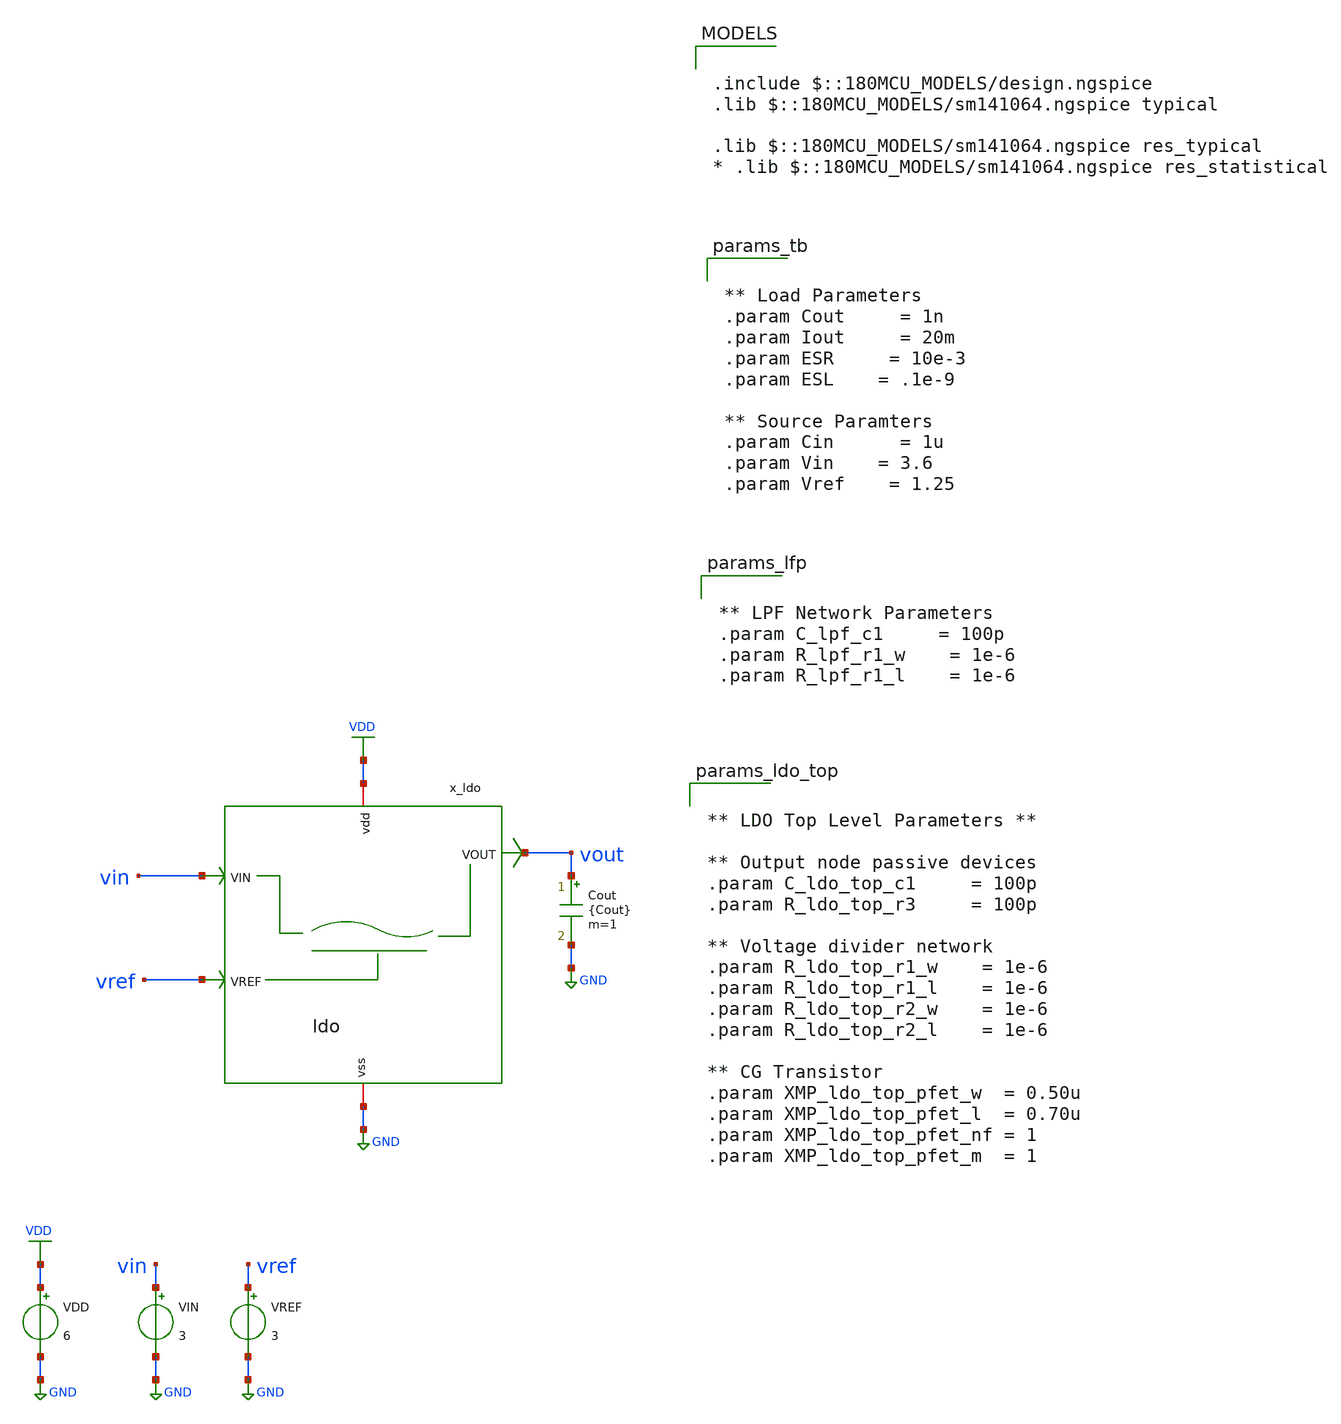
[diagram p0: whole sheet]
** sch_path: analog-db/circuits/ldo_005_buffered_ref/reference/ti-ldo/testbench/dc_trans_tb.sch
**.subckt dc_trans_tb
VDD VDD GND 6
VIN vin GND 3
VREF vref GND 3
Cout vout GND {Cout} m=1
x_ldo vout vin vref GND VDD ldo
**** begin user architecture code

.include $::180MCU_MODELS/design.ngspice
.lib $::180MCU_MODELS/sm141064.ngspice typical

.lib $::180MCU_MODELS/sm141064.ngspice res_typical
* .lib $::180MCU_MODELS/sm141064.ngspice res_statistical


** Load Parameters
.param Cout 	= 1n
.param Iout 	= 20m
.param ESR 	= 10e-3
.param ESL	= .1e-9

** Source Paramters
.param Cin  	= 1u
.param Vin	= 3.6
.param Vref	= 1.25



** LPF Network Parameters
.param C_lpf_c1 	= 100p
.param R_lpf_r1_w	= 1e-6
.param R_lpf_r1_l	= 1e-6



** LDO Top Level Parameters **

** Output node passive devices
.param C_ldo_top_c1 	= 100p
.param R_ldo_top_r3 	= 100p

** Voltage divider network
.param R_ldo_top_r1_w	= 1e-6
.param R_ldo_top_r1_l	= 1e-6
.param R_ldo_top_r2_w	= 1e-6
.param R_ldo_top_r2_l	= 1e-6

** CG Transistor
.param XMP_ldo_top_pfet_w  = 0.50u
.param XMP_ldo_top_pfet_l  = 0.70u
.param XMP_ldo_top_pfet_nf = 1
.param XMP_ldo_top_pfet_m  = 1




** Ref Amp Parameters **

.param I_ref_ref_amp = 1m


** Passive Devices
.param C_ref_amp_c1 	= 100p

.param R_ref_amp_r1_w	= 1e-6
.param R_ref_amp_r1_l	= 1e-6

** NMOS
** ref_amp.M1 Transistor
.param M1_ref_amp_nfet_w  = 0.50u
.param M1_ref_amp_nfet_l  = 0.30u
.param M1_ref_amp_nfet_nf = 1
.param M1_ref_amp_nfet_m  = 1

** ref_amp.M2 Transistor
.param M2_ref_amp_nfet_w  = 0.50u
.param M2_ref_amp_nfet_l  = 0.30u
.param M2_ref_amp_nfet_nf = 1
.param M2_ref_amp_nfet_m  = 1

** ref_amp.M_mirror_out Transistor
.param M_mirror_out_ref_amp_nfet_w  = 0.50u
.param M_mirror_out_ref_amp_nfet_l  = 0.30u
.param M_mirror_out_ref_amp_nfet_nf = 1
.param M_mirror_out_ref_amp_nfet_m  = 1

** ref_amp.M_mirror_a Transistor
.param M_mirror_a_ref_amp_nfet_w  = 0.50u
.param M_mirror_a_ref_amp_nfet_l  = 0.30u
.param M_mirror_a_ref_amp_nfet_nf = 1
.param M_mirror_a_ref_amp_nfet_m  = 1


** ref_amp.M_mirror_ref Transistor
.param M_mirror_ref_ref_amp_nfet_w  = 0.50u
.param M_mirror_ref_ref_amp_nfet_l  = 0.30u
.param M_mirror_ref_ref_amp_nfet_nf = 1
.param M_mirror_ref_ref_amp_nfet_m  = 1


** PMOS
** ref_amp.M3 Transistor
.param M3_ref_amp_pfet_w  = 0.50u
.param M3_ref_amp_pfet_l  = 0.30u
.param M3_ref_amp_pfet_nf = 1
.param M3_ref_amp_pfet_m  = 1


** ref_amp.M4 Transistor
.param M4_ref_amp_pfet_w  = 0.50u
.param M4_ref_amp_pfet_l  = 0.30u
.param M4_ref_amp_pfet_nf = 1
.param M4_ref_amp_pfet_m  = 1


** ref_amp.M5 Transistor
.param M5_ref_amp_pfet_w  = 0.50u
.param M5_ref_amp_pfet_l  = 0.30u
.param M5_ref_amp_pfet_nf = 1
.param M5_ref_amp_pfet_m  = 1



** Error Amp Parameters **

.param I_error_amp_ref = 1m


** Passive Devices
.param C_error_amp_cc 	= 100p

.param R_error_amp_rz_w	= 1e-6
.param R_error_amp_rz_l	= 1e-6

** NMOS
** error_amp.M1 Transistor
.param M1_error_amp_nfet_w  = 0.50u
.param M1_error_amp_nfet_l  = 0.30u
.param M1_error_amp_nfet_nf = 1
.param M1_error_amp_nfet_m  = 1

** error_amp.M2 Transistor
.param M2_error_amp_nfet_w  = 0.50u
.param M2_error_amp_nfet_l  = 0.30u
.param M2_error_amp_nfet_nf = 1
.param M2_error_amp_nfet_m  = 1

** error_amp.M_mirror_ea_out Transistor
.param M_mirror_ea_out_error_amp_nfet_w  = 0.50u
.param M_mirror_ea_out_error_amp_nfet_l  = 0.30u
.param M_mirror_ea_out_error_amp_nfet_nf = 1
.param M_mirror_ea_out_error_amp_nfet_m  = 1

** error_amp.M_mirror_e Transistor
.param M_mirror_e_error_amp_nfet_w  = 0.50u
.param M_mirror_e_error_amp_nfet_l  = 0.30u
.param M_mirror_e_error_amp_nfet_nf = 1
.param M_mirror_e_error_amp_nfet_m  = 1

** error_amp.M_mirror_c Transistor
.param M_mirror_c_error_amp_nfet_w  = 0.50u
.param M_mirror_c_error_amp_nfet_l  = 0.30u
.param M_mirror_c_error_amp_nfet_nf = 1
.param M_mirror_c_error_amp_nfet_m  = 1

** error_amp.M_mirror_f Transistor
.param M_mirror_f_error_amp_nfet_w  = 0.50u
.param M_mirror_f_error_amp_nfet_l  = 0.30u
.param M_mirror_f_error_amp_nfet_nf = 1
.param M_mirror_f_error_amp_nfet_m  = 1

** error_amp.M_mirror_error_amp_ref Transistor
.param M_mirror_error_amp_ref_error_amp_nfet_w  = 0.50u
.param M_mirror_error_amp_ref_error_amp_nfet_l  = 0.30u
.param M_mirror_error_amp_ref_error_amp_nfet_nf = 1
.param M_mirror_error_amp_ref_error_amp_nfet_m  = 1

** PMOS
** error_amp.M3 Transistor
.param M3_error_amp_pfet_w  = 0.50u
.param M3_error_amp_pfet_l  = 0.30u
.param M3_error_amp_pfet_nf = 1
.param M3_error_amp_pfet_m  = 1

** error_amp.M4 Transistor
.param M4_error_amp_pfet_w  = 0.50u
.param M4_error_amp_pfet_l  = 0.30u
.param M4_error_amp_pfet_nf = 1
.param M4_error_amp_pfet_m  = 1

** error_amp.M5 Transistor
.param M5_error_amp_pfet_w  = 0.50u
.param M5_error_amp_pfet_l  = 0.30u
.param M5_error_amp_pfet_nf = 1
.param M5_error_amp_pfet_m  = 1

** error_amp.M6 Transistor
.param M6_error_amp_pfet_w  = 0.50u
.param M6_error_amp_pfet_l  = 0.30u
.param M6_error_amp_pfet_nf = 1
.param M6_error_amp_pfet_m  = 1

** error_amp.M7 Transistor
.param M7_error_amp_pfet_w  = 0.50u
.param M7_error_amp_pfet_l  = 0.30u
.param M7_error_amp_pfet_nf = 1
.param M7_error_amp_pfet_m  = 1


**** end user architecture code
**.ends
.GLOBAL VDD
.GLOBAL GND
**** begin user architecture code



.control
save all

** VARIABLE DEFINITION
**   let allows defining vars that can be used in mathematicall expressions
**   set is only string variables

** Input Signal
let fsig = 1k
let tper = 1/fsig
** rise fall/time
let tfr  = 0.01*tper
let ton  = 0.5*tper-2*tfr

** Transient Params
let tstop = 2*tper
let tstep = 0.001*tper

** Set Sources
alter @VIN[DC] = 3.0
alter @VIN[PULSE] = [ 0 6 0 $&tfr $&tfr $&ton $&tper 0 ]
** $& is to convert the variables defined by let to string variables defined by set command

** Simulation
op
dc vin_p 0 3.3 0.01
tran $&tstep $&tstop

** Plots
let vout = v(vout)
let vea_out = v(x_ldo.ea_out)
plot vout vea_out

setplot tran1
let vout = v(vout)
let vin = v(vin)
let vref = v(vref)
let ivdd = -1 * vdd#branch * 1e4
let vea_out = v(x_ldo.ea_out)
plot vout vin vref vea_out
write tran.raw


** Reset plot so the save command uses the operating points
setplot op1
write op.raw
.endc


**** end user architecture code
.end
